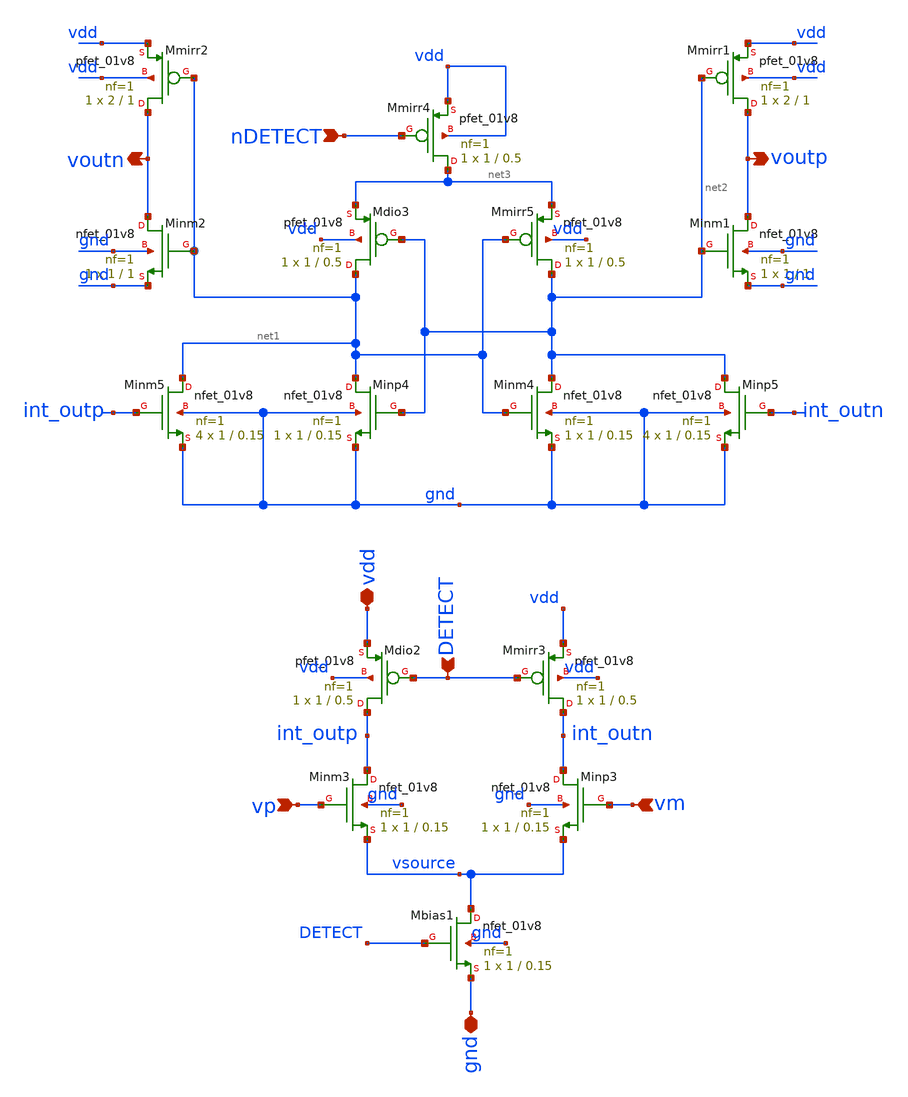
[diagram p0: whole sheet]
** sch_path: analog/xschem/col_amp_v2_std_dvs/xschem/dyn_comp.sch
**.subckt dyn_comp vdd gnd vp vm nDETECT voutn voutp DETECT
*.iopin vdd
*.iopin gnd
*.ipin vp
*.ipin vm
*.ipin nDETECT
*.opin voutn
*.opin voutp
*.ipin DETECT
XMmirr3 int_outn DETECT vdd vdd sky130_fd_pr__pfet_01v8 L=0.5 W=1 nf=1 ad='int((1 + 1)/2) * 1 / 1 * 0.29'
+ as='int((1 + 2)/2) * 1 / 1 * 0.29' pd='2*int((1 + 1)/2) * (1 / 1 + 0.29)' ps='2*int((1 + 2)/2) * (1 / 1 + 0.29)'
+ nrd='0.29 / 1 ' nrs='0.29 / 1 ' sa=0 sb=0 sd=0 mult=1 m=1
XMdio2 int_outp DETECT vdd vdd sky130_fd_pr__pfet_01v8 L=0.5 W=1 nf=1 ad='int((1 + 1)/2) * 1 / 1 * 0.29'
+ as='int((1 + 2)/2) * 1 / 1 * 0.29' pd='2*int((1 + 1)/2) * (1 / 1 + 0.29)' ps='2*int((1 + 2)/2) * (1 / 1 + 0.29)'
+ nrd='0.29 / 1 ' nrs='0.29 / 1 ' sa=0 sb=0 sd=0 mult=1 m=1
XMinm3 int_outp vp vsource gnd sky130_fd_pr__nfet_01v8 L=0.15 W=1 nf=1 ad='int((1 + 1)/2) * 1 / 1 * 0.29'
+ as='int((1 + 2)/2) * 1 / 1 * 0.29' pd='2*int((1 + 1)/2) * (1 / 1 + 0.29)' ps='2*int((1 + 2)/2) * (1 / 1 + 0.29)'
+ nrd='0.29 / 1 ' nrs='0.29 / 1 ' sa=0 sb=0 sd=0 mult=1 m=1
XMinp3 int_outn vm vsource gnd sky130_fd_pr__nfet_01v8 L=0.15 W=1 nf=1 ad='int((1 + 1)/2) * 1 / 1 * 0.29'
+ as='int((1 + 2)/2) * 1 / 1 * 0.29' pd='2*int((1 + 1)/2) * (1 / 1 + 0.29)' ps='2*int((1 + 2)/2) * (1 / 1 + 0.29)'
+ nrd='0.29 / 1 ' nrs='0.29 / 1 ' sa=0 sb=0 sd=0 mult=1 m=1
XMbias1 vsource DETECT gnd gnd sky130_fd_pr__nfet_01v8 L=0.15 W=1 nf=1 ad='int((1 + 1)/2) * 1 / 1 * 0.29'
+ as='int((1 + 2)/2) * 1 / 1 * 0.29' pd='2*int((1 + 1)/2) * (1 / 1 + 0.29)' ps='2*int((1 + 2)/2) * (1 / 1 + 0.29)'
+ nrd='0.29 / 1 ' nrs='0.29 / 1 ' sa=0 sb=0 sd=0 mult=1 m=1
XMmirr4 net3 nDETECT vdd vdd sky130_fd_pr__pfet_01v8 L=0.5 W=1 nf=1 ad='int((1 + 1)/2) * 1 / 1 * 0.29'
+ as='int((1 + 2)/2) * 1 / 1 * 0.29' pd='2*int((1 + 1)/2) * (1 / 1 + 0.29)' ps='2*int((1 + 2)/2) * (1 / 1 + 0.29)'
+ nrd='0.29 / 1 ' nrs='0.29 / 1 ' sa=0 sb=0 sd=0 mult=1 m=1
XMmirr5 net2 net1 net3 vdd sky130_fd_pr__pfet_01v8 L=0.5 W=1 nf=1 ad='int((1 + 1)/2) * 1 / 1 * 0.29'
+ as='int((1 + 2)/2) * 1 / 1 * 0.29' pd='2*int((1 + 1)/2) * (1 / 1 + 0.29)' ps='2*int((1 + 2)/2) * (1 / 1 + 0.29)'
+ nrd='0.29 / 1 ' nrs='0.29 / 1 ' sa=0 sb=0 sd=0 mult=1 m=1
XMdio3 net1 net2 net3 vdd sky130_fd_pr__pfet_01v8 L=0.5 W=1 nf=1 ad='int((1 + 1)/2) * 1 / 1 * 0.29' as='int((1 + 2)/2) * 1 / 1 * 0.29'
+ pd='2*int((1 + 1)/2) * (1 / 1 + 0.29)' ps='2*int((1 + 2)/2) * (1 / 1 + 0.29)' nrd='0.29 / 1 ' nrs='0.29 / 1 '
+ sa=0 sb=0 sd=0 mult=1 m=1
XMinp4 net1 net2 gnd gnd sky130_fd_pr__nfet_01v8 L=0.15 W=1 nf=1 ad='int((1 + 1)/2) * 1 / 1 * 0.29' as='int((1 + 2)/2) * 1 / 1 * 0.29'
+ pd='2*int((1 + 1)/2) * (1 / 1 + 0.29)' ps='2*int((1 + 2)/2) * (1 / 1 + 0.29)' nrd='0.29 / 1 ' nrs='0.29 / 1 '
+ sa=0 sb=0 sd=0 mult=1 m=1
XMinm4 net2 net1 gnd gnd sky130_fd_pr__nfet_01v8 L=0.15 W=1 nf=1 ad='int((1 + 1)/2) * 1 / 1 * 0.29' as='int((1 + 2)/2) * 1 / 1 * 0.29'
+ pd='2*int((1 + 1)/2) * (1 / 1 + 0.29)' ps='2*int((1 + 2)/2) * (1 / 1 + 0.29)' nrd='0.29 / 1 ' nrs='0.29 / 1 '
+ sa=0 sb=0 sd=0 mult=1 m=1
XMinm5 net1 int_outp gnd gnd sky130_fd_pr__nfet_01v8 L=0.15 W=1 nf=1 ad='int((1 + 1)/2) * 1 / 1 * 0.29'
+ as='int((1 + 2)/2) * 1 / 1 * 0.29' pd='2*int((1 + 1)/2) * (1 / 1 + 0.29)' ps='2*int((1 + 2)/2) * (1 / 1 + 0.29)'
+ nrd='0.29 / 1 ' nrs='0.29 / 1 ' sa=0 sb=0 sd=0 mult=4 m=4
XMinp5 net2 int_outn gnd gnd sky130_fd_pr__nfet_01v8 L=0.15 W=1 nf=1 ad='int((1 + 1)/2) * 1 / 1 * 0.29'
+ as='int((1 + 2)/2) * 1 / 1 * 0.29' pd='2*int((1 + 1)/2) * (1 / 1 + 0.29)' ps='2*int((1 + 2)/2) * (1 / 1 + 0.29)'
+ nrd='0.29 / 1 ' nrs='0.29 / 1 ' sa=0 sb=0 sd=0 mult=4 m=4
XMmirr1 voutp net2 vdd vdd sky130_fd_pr__pfet_01v8 L=1 W=2 nf=1 ad='int((1 + 1)/2) * 2 / 1 * 0.29' as='int((1 + 2)/2) * 2 / 1 * 0.29'
+ pd='2*int((1 + 1)/2) * (2 / 1 + 0.29)' ps='2*int((1 + 2)/2) * (2 / 1 + 0.29)' nrd='0.29 / 2 ' nrs='0.29 / 2 '
+ sa=0 sb=0 sd=0 mult=1 m=1
XMinm1 voutp net2 gnd gnd sky130_fd_pr__nfet_01v8 L=1 W=1 nf=1 ad='int((1 + 1)/2) * 1 / 1 * 0.29' as='int((1 + 2)/2) * 1 / 1 * 0.29'
+ pd='2*int((1 + 1)/2) * (1 / 1 + 0.29)' ps='2*int((1 + 2)/2) * (1 / 1 + 0.29)' nrd='0.29 / 1 ' nrs='0.29 / 1 '
+ sa=0 sb=0 sd=0 mult=1 m=1
XMmirr2 voutn net1 vdd vdd sky130_fd_pr__pfet_01v8 L=1 W=2 nf=1 ad='int((1 + 1)/2) * 2 / 1 * 0.29' as='int((1 + 2)/2) * 2 / 1 * 0.29'
+ pd='2*int((1 + 1)/2) * (2 / 1 + 0.29)' ps='2*int((1 + 2)/2) * (2 / 1 + 0.29)' nrd='0.29 / 2 ' nrs='0.29 / 2 '
+ sa=0 sb=0 sd=0 mult=1 m=1
XMinm2 voutn net1 gnd gnd sky130_fd_pr__nfet_01v8 L=1 W=1 nf=1 ad='int((1 + 1)/2) * 1 / 1 * 0.29' as='int((1 + 2)/2) * 1 / 1 * 0.29'
+ pd='2*int((1 + 1)/2) * (1 / 1 + 0.29)' ps='2*int((1 + 2)/2) * (1 / 1 + 0.29)' nrd='0.29 / 1 ' nrs='0.29 / 1 '
+ sa=0 sb=0 sd=0 mult=1 m=1
**.ends
.end
